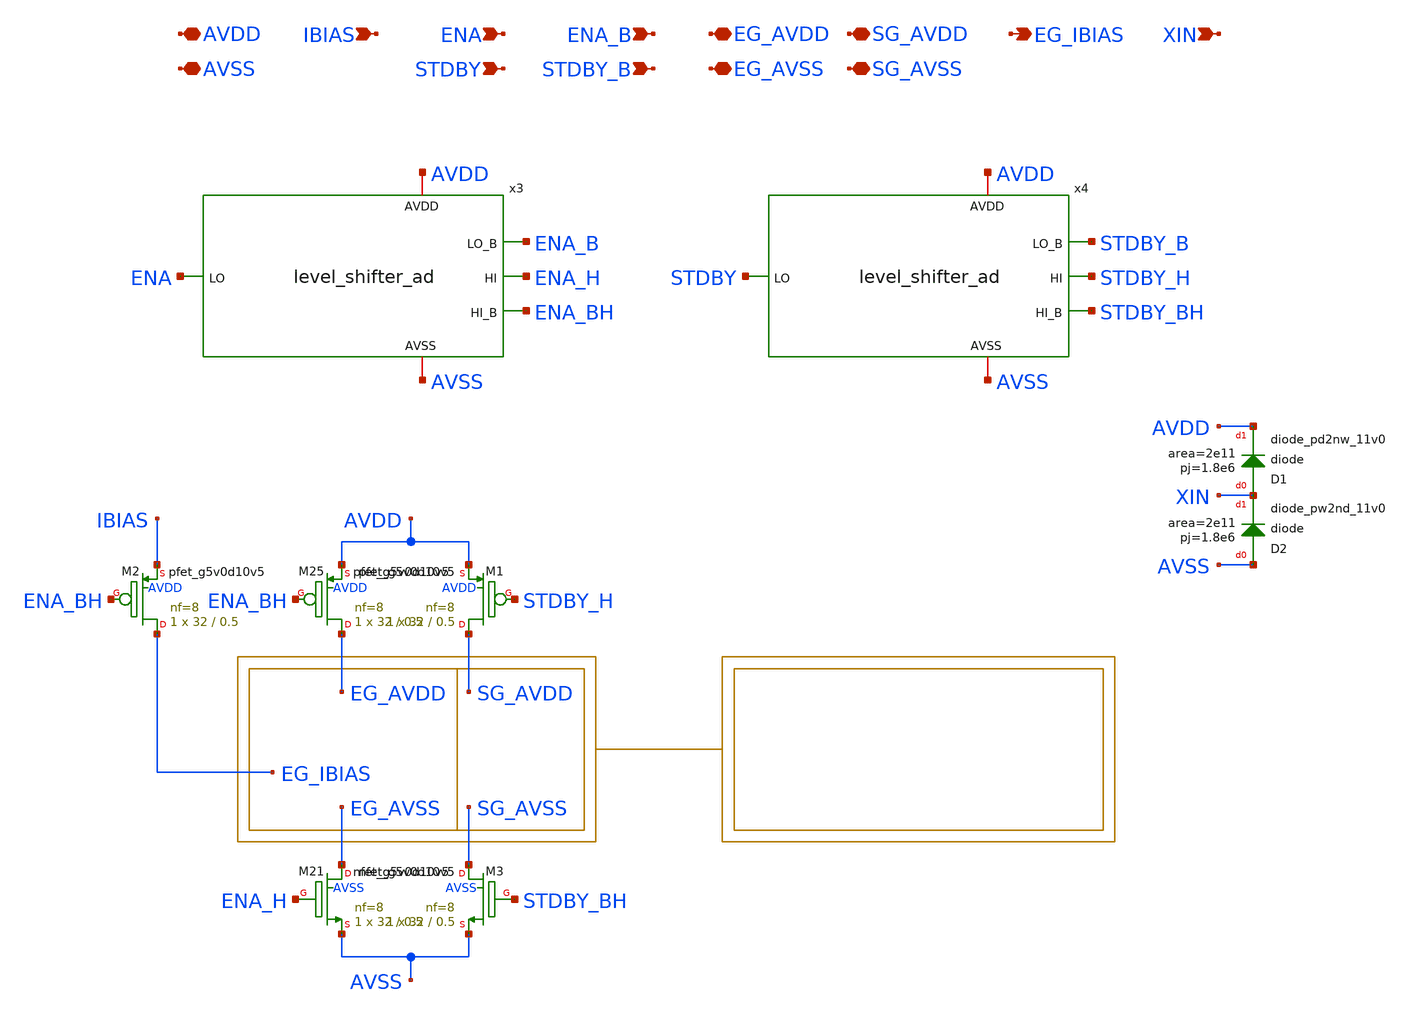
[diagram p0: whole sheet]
** sch_path: xschem/power_gating_ad.sch
**.subckt power_gating_ad AVDD AVSS ENA STDBY IBIAS EG_AVDD EG_AVSS SG_AVDD SG_AVSS EG_IBIAS XIN
*+ ENA_B STDBY_B
*.iopin AVDD
*.iopin AVSS
*.ipin ENA
*.ipin STDBY
*.ipin IBIAS
*.iopin EG_AVDD
*.iopin EG_AVSS
*.iopin SG_AVDD
*.iopin SG_AVSS
*.opin EG_IBIAS
*.ipin XIN
*.ipin ENA_B
*.ipin STDBY_B
x3 AVDD ENA_B ENA ENA_H AVSS ENA_BH level_shifter_ad
x4 AVDD STDBY_B STDBY STDBY_H AVSS STDBY_BH level_shifter_ad
XM21 EG_AVSS ENA_H AVSS AVSS sky130_fd_pr__nfet_g5v0d10v5 L=0.5 W=32 nf=8 ad='int((nf+1)/2) * W/nf * 0.29'
+ as='int((nf+2)/2) * W/nf * 0.29' pd='2*int((nf+1)/2) * (W/nf + 0.29)' ps='2*int((nf+2)/2) * (W/nf + 0.29)'
+ nrd='0.29 / W' nrs='0.29 / W' sa=0 sb=0 sd=0 mult=1 m=1
XM25 EG_AVDD ENA_BH AVDD AVDD sky130_fd_pr__pfet_g5v0d10v5 L=0.5 W=32 nf=8 ad='int((nf+1)/2) * W/nf * 0.29'
+ as='int((nf+2)/2) * W/nf * 0.29' pd='2*int((nf+1)/2) * (W/nf + 0.29)' ps='2*int((nf+2)/2) * (W/nf + 0.29)'
+ nrd='0.29 / W' nrs='0.29 / W' sa=0 sb=0 sd=0 mult=1 m=1
XM1 SG_AVDD STDBY_H AVDD AVDD sky130_fd_pr__pfet_g5v0d10v5 L=0.5 W=32 nf=8 ad='int((nf+1)/2) * W/nf * 0.29'
+ as='int((nf+2)/2) * W/nf * 0.29' pd='2*int((nf+1)/2) * (W/nf + 0.29)' ps='2*int((nf+2)/2) * (W/nf + 0.29)'
+ nrd='0.29 / W' nrs='0.29 / W' sa=0 sb=0 sd=0 mult=1 m=1
XM2 EG_IBIAS ENA_BH IBIAS AVDD sky130_fd_pr__pfet_g5v0d10v5 L=0.5 W=32 nf=8 ad='int((nf+1)/2) * W/nf * 0.29'
+ as='int((nf+2)/2) * W/nf * 0.29' pd='2*int((nf+1)/2) * (W/nf + 0.29)' ps='2*int((nf+2)/2) * (W/nf + 0.29)'
+ nrd='0.29 / W' nrs='0.29 / W' sa=0 sb=0 sd=0 mult=1 m=1
XM3 SG_AVSS STDBY_BH AVSS AVSS sky130_fd_pr__nfet_g5v0d10v5 L=0.5 W=32 nf=8 ad='int((nf+1)/2) * W/nf * 0.29'
+ as='int((nf+2)/2) * W/nf * 0.29' pd='2*int((nf+1)/2) * (W/nf + 0.29)' ps='2*int((nf+2)/2) * (W/nf + 0.29)'
+ nrd='0.29 / W' nrs='0.29 / W' sa=0 sb=0 sd=0 mult=1 m=1
XD1 XIN AVDD sky130_fd_pr__diode_pd2nw_11v0 area=2e11 pj=1.8e6
XD2 AVSS XIN sky130_fd_pr__diode_pw2nd_11v0 area=2e11 pj=1.8e6
**.ends

* expanding   symbol:  level_shifter_ad.sym # of pins=6
** sym_path: xschem/level_shifter_ad.sym
** sch_path: xschem/level_shifter_ad.sch
.subckt level_shifter_ad AVDD LO_B LO HI AVSS HI_B
*.iopin AVDD
*.iopin AVSS
*.ipin LO
*.opin HI
*.opin HI_B
*.ipin LO_B
XM21 HI_B LO AVSS AVSS sky130_fd_pr__nfet_g5v0d10v5 L=0.5 W=1 nf=1 ad='int((nf+1)/2) * W/nf * 0.29' as='int((nf+2)/2) * W/nf * 0.29'
+ pd='2*int((nf+1)/2) * (W/nf + 0.29)' ps='2*int((nf+2)/2) * (W/nf + 0.29)' nrd='0.29 / W' nrs='0.29 / W'
+ sa=0 sb=0 sd=0 mult=1 m=1
XM25 HI_B HI AVDD AVDD sky130_fd_pr__pfet_g5v0d10v5 L=0.5 W=1 nf=1 ad='int((nf+1)/2) * W/nf * 0.29' as='int((nf+2)/2) * W/nf * 0.29'
+ pd='2*int((nf+1)/2) * (W/nf + 0.29)' ps='2*int((nf+2)/2) * (W/nf + 0.29)' nrd='0.29 / W' nrs='0.29 / W'
+ sa=0 sb=0 sd=0 mult=1 m=1
XM1 HI HI_B AVDD AVDD sky130_fd_pr__pfet_g5v0d10v5 L=0.5 W=1 nf=1 ad='int((nf+1)/2) * W/nf * 0.29' as='int((nf+2)/2) * W/nf * 0.29'
+ pd='2*int((nf+1)/2) * (W/nf + 0.29)' ps='2*int((nf+2)/2) * (W/nf + 0.29)' nrd='0.29 / W' nrs='0.29 / W'
+ sa=0 sb=0 sd=0 mult=1 m=1
XM2 HI LO_B AVSS AVSS sky130_fd_pr__nfet_g5v0d10v5 L=0.5 W=1 nf=1 ad='int((nf+1)/2) * W/nf * 0.29' as='int((nf+2)/2) * W/nf * 0.29'
+ pd='2*int((nf+1)/2) * (W/nf + 0.29)' ps='2*int((nf+2)/2) * (W/nf + 0.29)' nrd='0.29 / W' nrs='0.29 / W'
+ sa=0 sb=0 sd=0 mult=1 m=1
.ends

.end
